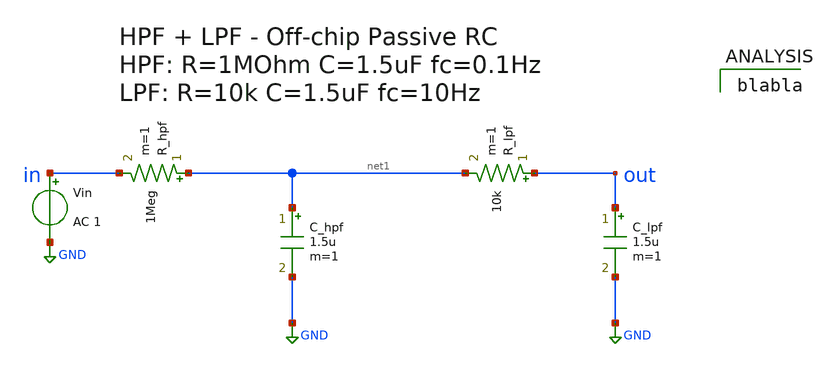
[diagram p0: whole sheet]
** sch_path: ps-filters/filters.sch
**.subckt filters
Vin in GND AC 1
R_hpf net1 in 1Meg m=1
C_hpf net1 GND 1.5u m=1
R_lpf out net1 10k m=1
C_lpf out GND 1.5u m=1
**** begin user architecture code

blabla

**** end user architecture code
**.ends
.GLOBAL GND
.end
